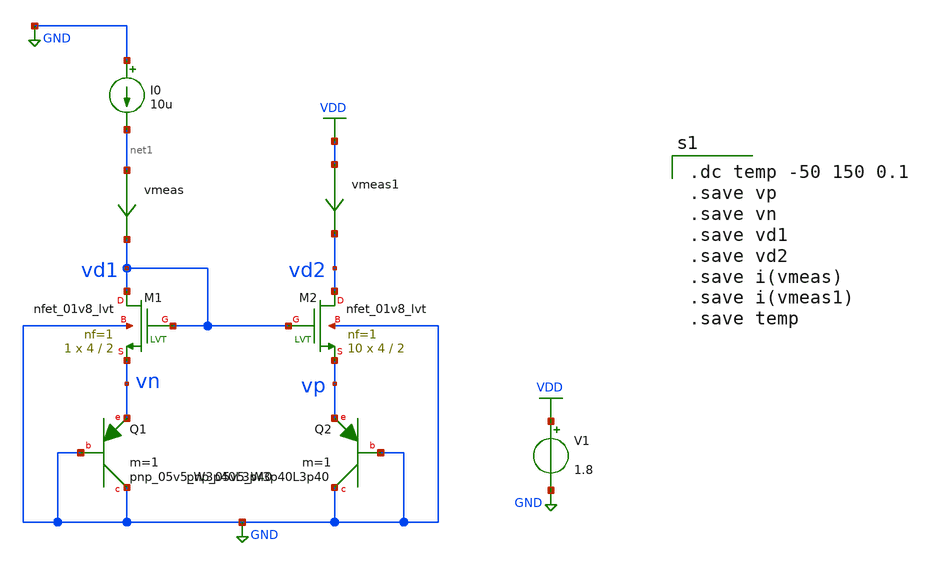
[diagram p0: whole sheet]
** sch_path: XSCHEM/PTAT_voltage_generator_design_tb.sch
**.subckt PTAT_voltage_generator_design_tb
XM1 vd1 vd1 vn GND sky130_fd_pr__nfet_01v8_lvt L=2 W=4 nf=1 ad='int((nf+1)/2) * W/nf * 0.29' as='int((nf+2)/2) * W/nf * 0.29'
+ pd='2*int((nf+1)/2) * (W/nf + 0.29)' ps='2*int((nf+2)/2) * (W/nf + 0.29)' nrd='0.29 / W' nrs='0.29 / W'
+ sa=0 sb=0 sd=0 mult=1 m=1
XQ1 GND GND vn sky130_fd_pr__pnp_05v5_W3p40L3p40 m=1
XM2 vd2 vd1 vp GND sky130_fd_pr__nfet_01v8_lvt L=2 W=4 nf=1 ad='int((nf+1)/2) * W/nf * 0.29' as='int((nf+2)/2) * W/nf * 0.29'
+ pd='2*int((nf+1)/2) * (W/nf + 0.29)' ps='2*int((nf+2)/2) * (W/nf + 0.29)' nrd='0.29 / W' nrs='0.29 / W'
+ sa=0 sb=0 sd=0 mult=10 m=10
XQ2 GND GND vp sky130_fd_pr__pnp_05v5_W3p40L3p40 m=1
V1 VDD GND 1.8
vmeas1 VDD vd2 0
.save i(vmeas1)
vmeas net1 vd1 0
.save i(vmeas)
I0 GND net1 10u
**** begin user architecture code

.dc temp -50 150 0.1
.save vp
.save vn
.save vd1
.save vd2
.save i(vmeas)
.save i(vmeas1)
.save temp


** opencircuitdesign pdks install
.lib $::SKYWATER_MODELS/sky130.lib.spice tt


**** end user architecture code
**.ends
.GLOBAL GND
.GLOBAL VDD
.end
